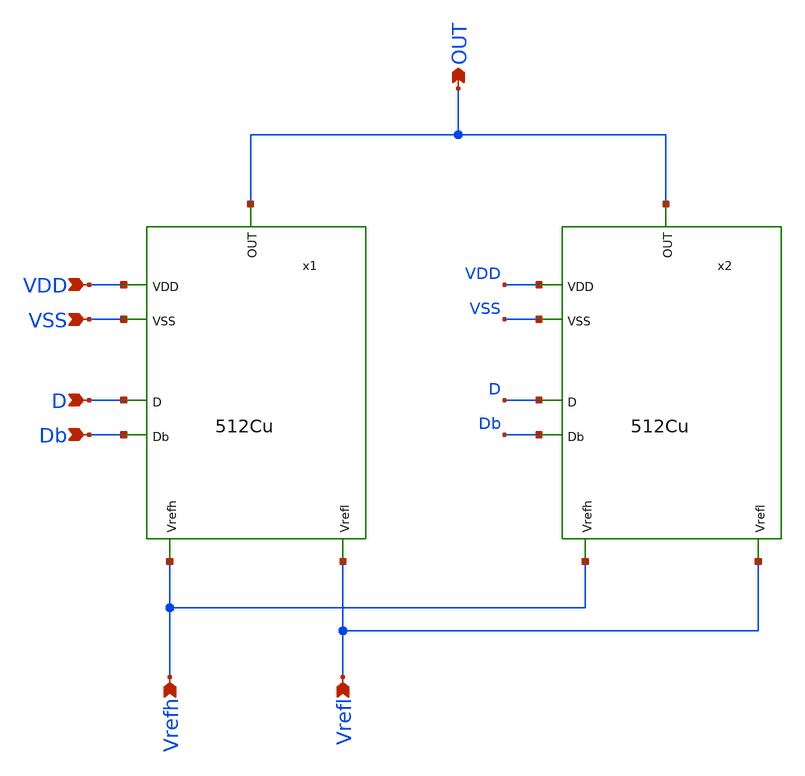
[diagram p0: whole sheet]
** sch_path: 1024Cu.sch
**.subckt 1024Cu OUT VDD D VSS Vrefh Vrefl Db
*.opin OUT
*.ipin VDD
*.ipin D
*.ipin VSS
*.ipin Vrefh
*.ipin Vrefl
*.ipin Db
x1 OUT VSS VDD Db D Vrefl Vrefh 512Cu
x2 OUT VSS VDD Db D Vrefl Vrefh 512Cu
**.ends
.end
